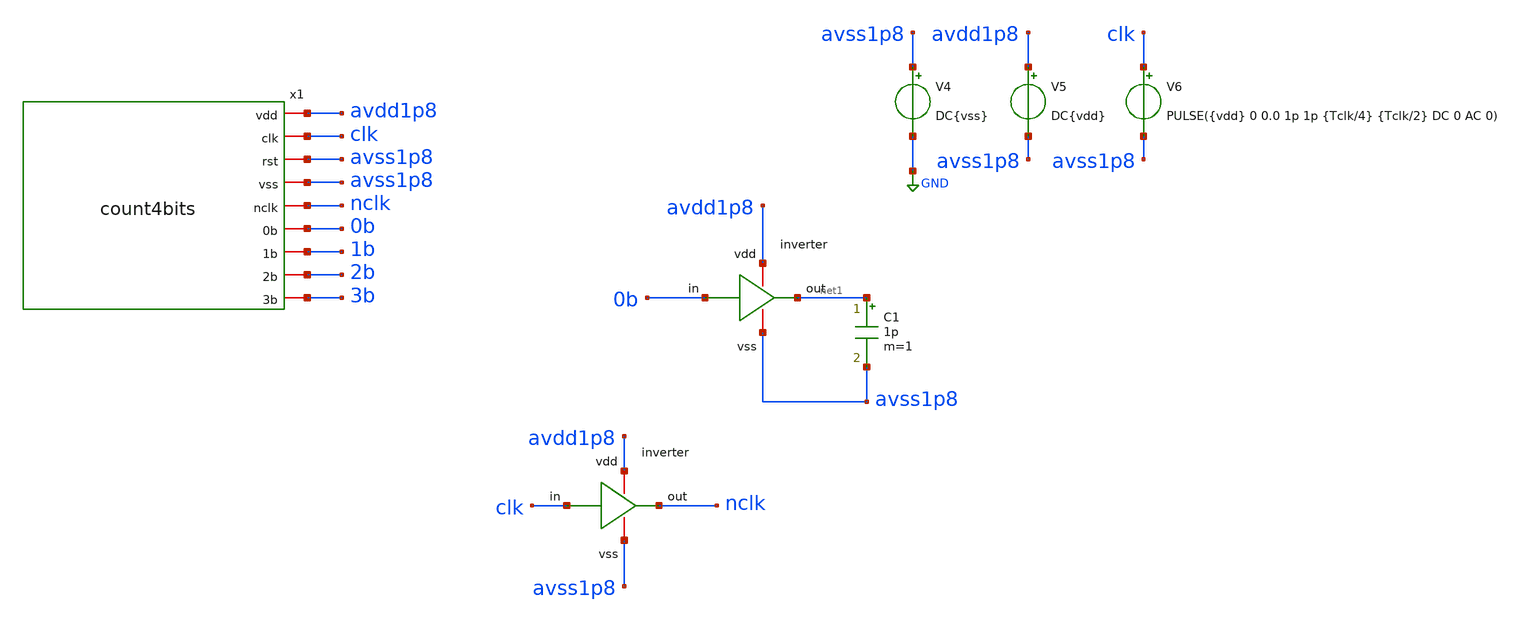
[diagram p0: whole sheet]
** sch_path: verification/testbenches/tb_count4bits.sch
**.subckt tb_count4bits
C1 net1 avss1p8 1p m=1
V4 avss1p8 GND DC{vss}
V5 avdd1p8 avss1p8 DC{vdd}
V6 clk avss1p8 PULSE({vdd} 0 0.0 1p 1p {Tclk/4} {Tclk/2} DC 0 AC 0)
x2 avdd1p8 net1 0b avss1p8 inverter
x3 avdd1p8 nclk clk avss1p8 inverter
x1 avdd1p8 clk avss1p8 avss1p8 nclk 0b 1b 2b 3b count4bits
**** begin user architecture code


* Circuit Parameters
.param vdd = 1.2
.param vss = 0.0
.param Tclk = 10n
.options TEMP = 27.0
* Include Models - IHP SG13G2
.lib cornerMOSlv.lib mos_tt
* OP Parameters & Singals to save
.save all
*Simulations
.control
tran 0.01u 100n
setplot tran1
plot v(clk) v(0b)+1.2 v(1b)+2.4 v(2b)+3.6 v(3b)+4.8
reset
dc V6 0 1.2 0.01
setplot dc
set filetype = ascii
write dcsweep.raw
.endc
.end


**** end user architecture code
**.ends

* expanding   symbol:  blocks/inverter/schematic/inverter.sym # of pins=4
** sym_path: design/blocks/inverter/schematic/inverter.sym
** sch_path: design/blocks/inverter/schematic/inverter.sch
.subckt inverter vdd out in vss
*.iopin vdd
*.iopin out
*.iopin vss
*.iopin in
XM1 out in vss vss sky130_fd_pr__nfet_01v8 L=0.15 W=0.75 nf=1 ad='int((nf+1)/2) * W/nf * 0.29' as='int((nf+2)/2) * W/nf * 0.29'
+ pd='2*int((nf+1)/2) * (W/nf + 0.29)' ps='2*int((nf+2)/2) * (W/nf + 0.29)' nrd='0.29 / W' nrs='0.29 / W'
+ sa=0 sb=0 sd=0 mult=1 m=1
XM2 out in vdd vdd sky130_fd_pr__pfet_01v8 L=0.15 W=1.5 nf=1 ad='int((nf+1)/2) * W/nf * 0.29' as='int((nf+2)/2) * W/nf * 0.29'
+ pd='2*int((nf+1)/2) * (W/nf + 0.29)' ps='2*int((nf+2)/2) * (W/nf + 0.29)' nrd='0.29 / W' nrs='0.29 / W'
+ sa=0 sb=0 sd=0 mult=1 m=1
.ends


* expanding   symbol:  blocks/count4bits/schematic/count4bits.sym # of pins=9
** sym_path: design/blocks/count4bits/schematic/count4bits.sym
** sch_path: design/blocks/count4bits/schematic/count4bits.sch
.subckt count4bits vdd clk rst vss nclk 0b 1b 2b 3b
*.iopin vdd
*.iopin clk
*.iopin rst
*.iopin vss
*.iopin nclk
*.iopin 0b
*.iopin 1b
*.iopin 2b
*.iopin 3b
x1 vdd clk vdd 0b rst vss nclk count1bit
x2 vdd clk 0b 1b rst vss nclk count1bit
x3 vdd clk 1b 2b rst vss nclk count1bit
x4 vdd clk 2b 3b rst vss nclk count1bit
.ends


* expanding   symbol:  blocks/count1bit/schematic/count1bit.sym # of pins=7
** sym_path: design/blocks/count1bit/schematic/count1bit.sym
** sch_path: design/blocks/count1bit/schematic/count1bit.sch
.subckt count1bit vdd clk in out rst vss nlck
*.iopin in
*.iopin nlck
*.iopin clk
*.iopin out
*.iopin rst
*.iopin vss
*.iopin vdd
x2 net2 vdd in vss net1 xorgate
x3 clk nlck vss vdd net2 net1 rst register
x1 vdd net2 in out vss andgate
.ends


* expanding   symbol:  blocks/xorgate/schematic/xorgate.sym # of pins=5
** sym_path: design/blocks/xorgate/schematic/xorgate.sym
** sch_path: design/blocks/xorgate/schematic/xorgate.sch
.subckt xorgate a vdd b vss out
*.iopin a
*.iopin b
*.iopin vdd
*.iopin vss
*.iopin out
XM3 out a net1 vdd sg13_lv_pmos w=1.5u l=0.15u ng=1 m=1 mm_ok=1
XM1 out b net1 vdd sg13_lv_pmos w=1.5u l=0.15u ng=1 m=1 mm_ok=1
XM4 out na net2 vss sg13_lv_nmos w=1.5u l=0.15u ng=1 m=1 mm_ok=1
x1 vdd nb b vss inverter
x2 vdd na a vss inverter
XM2 net1 nb vdd vdd sg13_lv_pmos w=1.5u l=0.15u ng=1 m=1 mm_ok=1
XM5 net1 na vdd vdd sg13_lv_pmos w=1.5u l=0.15u ng=1 m=1 mm_ok=1
XM7 out a net3 vss sg13_lv_nmos w=1.5u l=0.15u ng=1 m=1 mm_ok=1
XM8 net2 nb vss vss sg13_lv_nmos w=1.5u l=0.15u ng=1 m=1 mm_ok=1
XM9 net3 b vss vss sg13_lv_nmos w=1.5u l=0.15u ng=1 m=1 mm_ok=1
.ends


* expanding   symbol:  blocks/register/schematic/register.sym # of pins=7
** sym_path: design/blocks/register/schematic/register.sym
** sch_path: design/blocks/register/schematic/register.sch
.subckt register en noten vss vdd out in rst
*.iopin in
*.iopin vdd
*.iopin vss
*.iopin en
*.iopin noten
*.iopin out
*.iopin rst
x1 vdd net1 in vss inverter
x3 vdd net3 net2 vss inverter
x4 vdd net4 net3 vss inverter
x5 net1 vdd noten net2 vss en transmissiongate
x6 net4 vdd en net2 vss noten transmissiongate
x2 vss vdd nrst net3 vss rst transmissiongate
x8 vss nrst rst vss inverter
x7 vdd net5 net3 vss inverter
x9 vdd out net6 vss inverter
x10 vdd net7 out vss inverter
x11 net5 vdd en net6 vss noten transmissiongate
x12 net7 vdd noten net6 vss en transmissiongate
x13 vss vdd nrst out vss rst transmissiongate
.ends


* expanding   symbol:  blocks/andgate/schematic/andgate.sym # of pins=5
** sym_path: design/blocks/andgate/schematic/andgate.sym
** sch_path: design/blocks/andgate/schematic/andgate.sch
.subckt andgate vdd a b out vss
*.iopin b
*.iopin a
*.iopin vdd
*.iopin vss
*.iopin out
XM1 net1 b vss vss sg13_lv_nmos w=1.5u l=0.15u ng=1 m=1 mm_ok=1
XM4 net2 a vdd vdd sg13_lv_pmos w=1.5u l=0.15u ng=1 m=1 mm_ok=1
x1 vdd out net2 vss inverter
XM3 net2 a net1 vss sg13_lv_nmos w=1.5u l=0.15u ng=1 m=1 mm_ok=1
XM5 net2 b vdd vdd sg13_lv_pmos w=1.5u l=0.15u ng=1 m=1 mm_ok=1
.ends


* expanding   symbol:  blocks/transmissiongate/schematic/transmissiongate.sym # of pins=6
** sym_path: design/blocks/transmissiongate/schematic/transmissiongate.sym
** sch_path: design/blocks/transmissiongate/schematic/transmissiongate.sch
.subckt transmissiongate in vdd noten out vss en
*.iopin noten
*.iopin en
*.iopin in
*.iopin out
*.iopin vdd
*.iopin vss
XM1 out noten in vdd sg13_lv_pmos w=1.5u l=0.15u ng=1 m=1 mm_ok=1
XM2 out en in vss sg13_lv_nmos w=0.75u l=0.15u ng=1 m=1 mm_ok=1
.ends

.GLOBAL GND
.end
